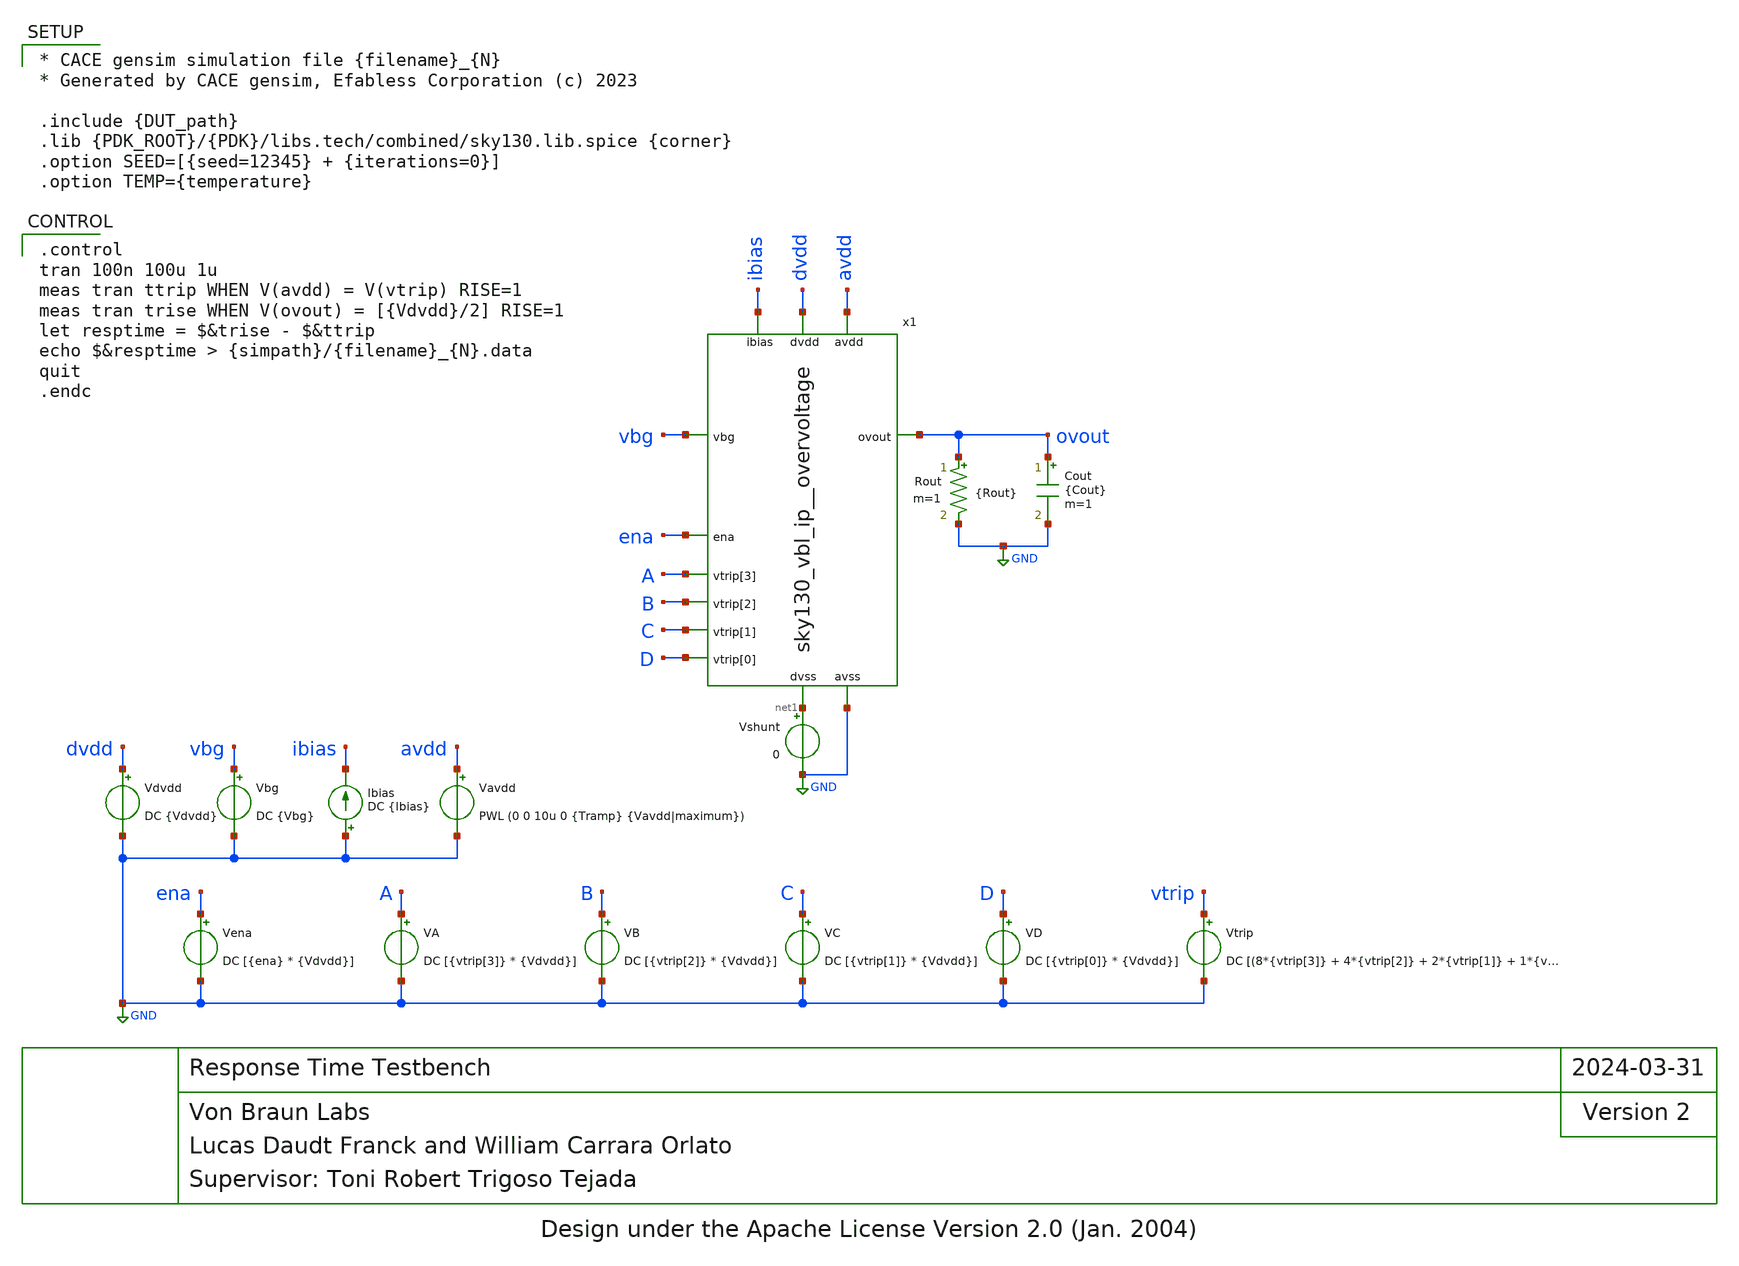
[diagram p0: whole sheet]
** sch_path: cace/tb_resptime.sch
* Design under the Apache License Version 2.0 (Jan. 2004)
**.subckt tb_resptime
Vavdd avdd GND PWL (0 0 10u 0 {Tramp} {Vavdd|maximum})
Vdvdd dvdd GND DC {Vdvdd}
Vbg vbg GND DC {Vbg}
Ibias GND ibias DC {Ibias}
Vena ena GND DC [{ena} * {Vdvdd}]
VA A GND DC [{vtrip[3]} * {Vdvdd}]
VB B GND DC [{vtrip[2]} * {Vdvdd}]
VC C GND DC [{vtrip[1]} * {Vdvdd}]
VD D GND DC [{vtrip[0]} * {Vdvdd}]
Cout ovout GND {Cout} m=1
Rout ovout GND {Rout} m=1
Vtrip vtrip GND DC [(8*{vtrip[3]} + 4*{vtrip[2]} + 2*{vtrip[1]} + 1*{vtrip[0]})*0.14667 + 3.3]
x1 avdd dvdd ena A ibias B ovout vbg C D net1 GND sky130_vbl_ip__overvoltage
Vshunt net1 GND 0
**** begin user architecture code

* CACE gensim simulation file {filename}_{N}
* Generated by CACE gensim, Efabless Corporation (c) 2023

.include {DUT_path}
.lib {PDK_ROOT}/{PDK}/libs.tech/combined/sky130.lib.spice {corner}
.option SEED=[{seed=12345} + {iterations=0}]
.option TEMP={temperature}



.control
tran 100n 100u 1u
meas tran ttrip WHEN V(avdd) = V(vtrip) RISE=1
meas tran trise WHEN V(ovout) = [{Vdvdd}/2] RISE=1
let resptime = $&trise - $&ttrip
echo $&resptime > {simpath}/{filename}_{N}.data
quit
.endc


**** end user architecture code
**.ends
.GLOBAL GND
.end
